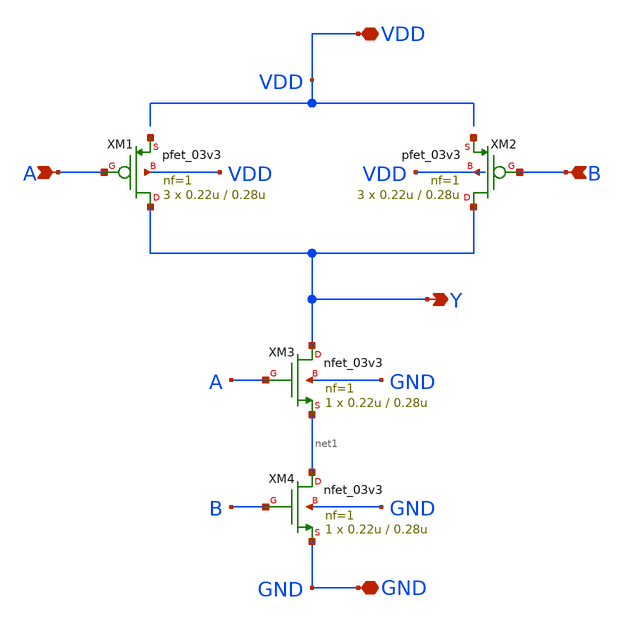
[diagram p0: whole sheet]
** sch_path: PFD/NAND.sch
**.subckt NAND Y A B VDD GND
*.opin Y
*.ipin A
*.ipin B
*.iopin VDD
*.iopin GND
XM1 Y A net2 VDD pfet_03v3 L=0.28u W=0.22u nf=1 ad='int((nf+1)/2) * W/nf * 0.18u' as='int((nf+2)/2) * W/nf * 0.18u'
+ pd='2*int((nf+1)/2) * (W/nf + 0.18u)' ps='2*int((nf+2)/2) * (W/nf + 0.18u)' nrd='0.18u / W' nrs='0.18u / W'
+ sa=0 sb=0 sd=0 m=3
XM3 Y A net1 GND nfet_03v3 L=0.28u W=0.22u nf=1 ad='int((nf+1)/2) * W/nf * 0.18u' as='int((nf+2)/2) * W/nf * 0.18u'
+ pd='2*int((nf+1)/2) * (W/nf + 0.18u)' ps='2*int((nf+2)/2) * (W/nf + 0.18u)' nrd='0.18u / W' nrs='0.18u / W'
+ sa=0 sb=0 sd=0 m=1
XM4 net1 B GND GND nfet_03v3 L=0.28u W=0.22u nf=1 ad='int((nf+1)/2) * W/nf * 0.18u' as='int((nf+2)/2) * W/nf * 0.18u'
+ pd='2*int((nf+1)/2) * (W/nf + 0.18u)' ps='2*int((nf+2)/2) * (W/nf + 0.18u)' nrd='0.18u / W' nrs='0.18u / W'
+ sa=0 sb=0 sd=0 m=1
XM2 Y B net3 VDD pfet_03v3 L=0.28u W=0.22u nf=1 ad='int((nf+1)/2) * W/nf * 0.18u' as='int((nf+2)/2) * W/nf * 0.18u'
+ pd='2*int((nf+1)/2) * (W/nf + 0.18u)' ps='2*int((nf+2)/2) * (W/nf + 0.18u)' nrd='0.18u / W' nrs='0.18u / W'
+ sa=0 sb=0 sd=0 m=3
**.ends
.end
